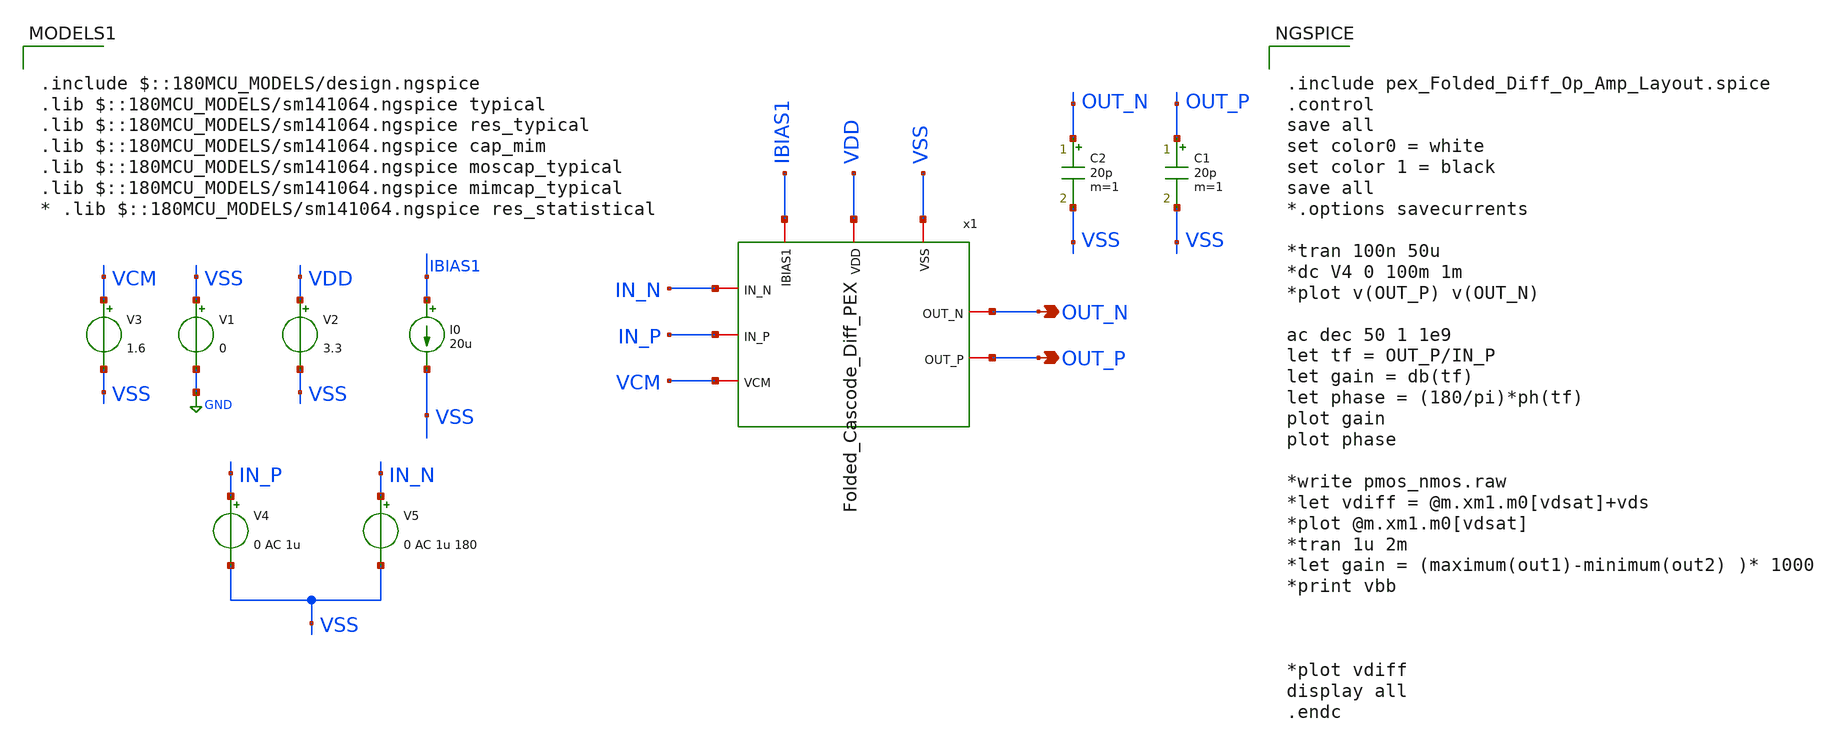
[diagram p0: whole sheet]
** sch_path: AWG_OUTPUT_AND_MUX_PAKISTAN_05/xschem/Folded_Cascode_Diff_TB.sch
**.subckt Folded_Cascode_Diff_TB OUT_N OUT_P
*.opin OUT_N
*.opin OUT_P
V1 VSS GND 0
V2 VDD VSS 3.3
V3 VCM VSS 1.6
I0 IBIAS1 VSS 20u
V4 IN_P VSS 0 AC 1u
V5 IN_N VSS 0 AC 1u 180
C1 OUT_P VSS 20p m=1
C2 OUT_N VSS 20p m=1
x1 VDD VSS IN_N IN_P IBIAS1 VCM OUT_N OUT_P Folded_Cascode_Diff_PEX
**** begin user architecture code


.include pex_Folded_Diff_Op_Amp_Layout.spice
.control
save all
set color0 = white
set color 1 = black
save all
*.options savecurrents

*tran 100n 50u
*dc V4 0 100m 1m
*plot v(OUT_P) v(OUT_N)

ac dec 50 1 1e9
let tf = OUT_P/IN_P
let gain = db(tf)
let phase = (180/pi)*ph(tf)
plot gain
plot phase

*write pmos_nmos.raw
*let vdiff = @m.xm1.m0[vdsat]+vds
*plot @m.xm1.m0[vdsat]
*tran 1u 2m
*let gain = (maximum(out1)-minimum(out2) )* 1000
*print vbb



*plot vdiff
display all
.endc



.include $::180MCU_MODELS/design.ngspice
.lib $::180MCU_MODELS/sm141064.ngspice typical
.lib $::180MCU_MODELS/sm141064.ngspice res_typical
.lib $::180MCU_MODELS/sm141064.ngspice cap_mim
.lib $::180MCU_MODELS/sm141064.ngspice moscap_typical
.lib $::180MCU_MODELS/sm141064.ngspice mimcap_typical
* .lib $::180MCU_MODELS/sm141064.ngspice res_statistical

**** end user architecture code
**.ends
.GLOBAL GND
.end
